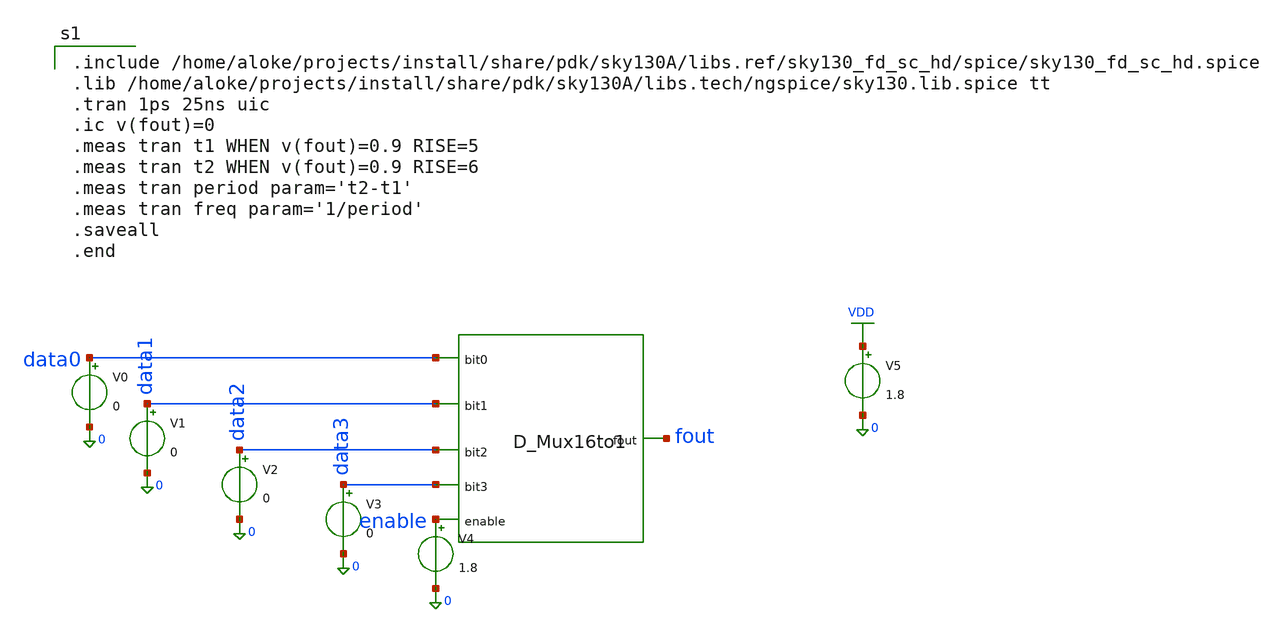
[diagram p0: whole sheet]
** sch_path: xschem/D_Mux16to1_tb.sch
**.subckt D_Mux16to1_tb
x1 data0 data1 enable data2 data3 fout D_Mux16to1
V0 data0 0 0
V1 data1 0 0
V2 data2 0 0
V3 data3 0 0
V5 VDD 0 1.8
V4 enable 0 1.8
**** begin user architecture code

.include /home/aloke/projects/install/share/pdk/sky130A/libs.ref/sky130_fd_sc_hd/spice/sky130_fd_sc_hd.spice
.lib /home/aloke/projects/install/share/pdk/sky130A/libs.tech/ngspice/sky130.lib.spice tt
.tran 1ps 25ns uic
.ic v(fout)=0
.meas tran t1 WHEN v(fout)=0.9 RISE=5
.meas tran t2 WHEN v(fout)=0.9 RISE=6
.meas tran period param='t2-t1'
.meas tran freq param='1/period'
.saveall
.end


**** end user architecture code
**.ends

* expanding   symbol:  D_Mux16to1.sym # of pins=6
** sym_path: xschem/D_Mux16to1.sym
** sch_path: xschem/D_Mux16to1.sch
.subckt D_Mux16to1 bit0 bit1 enable bit2 bit3 fout
*.ipin bit0
*.ipin bit1
*.ipin enable
*.ipin bit2
*.ipin bit3
*.opin fout
x37 net21 net22 net23 net24 net3 net4 VSS VSS VDD VDD net5 sky130_fd_sc_hd__mux4_1
x40 bit0 enable VSS VSS VDD VDD net3 sky130_fd_sc_hd__dlxtp_1
x1 fout VSS VSS VDD VDD net25 sky130_fd_sc_hd__clkinv_1
x36 net17 net18 net19 net20 net3 net4 VSS VSS VDD VDD net6 sky130_fd_sc_hd__mux4_1
x35 net13 net14 net15 net16 net3 net4 VSS VSS VDD VDD net7 sky130_fd_sc_hd__mux4_1
x34 net9 net10 net11 net12 net3 net4 VSS VSS VDD VDD net8 sky130_fd_sc_hd__mux4_1
x38 net8 net7 net6 net5 net1 net2 VSS VSS VDD VDD fout sky130_fd_sc_hd__mux4_1
x41 bit1 enable VSS VSS VDD VDD net4 sky130_fd_sc_hd__dlxtp_1
x42 bit2 enable VSS VSS VDD VDD net1 sky130_fd_sc_hd__dlxtp_1
x43 bit3 enable VSS VSS VDD VDD net2 sky130_fd_sc_hd__dlxtp_1
x2 net25 VSS VSS VDD VDD net26 sky130_fd_sc_hd__clkinv_1
x3 net26 VSS VSS VDD VDD net9 sky130_fd_sc_hd__clkinv_1
x4 net9 VSS VSS VDD VDD net27 sky130_fd_sc_hd__clkinv_1
x5 net27 VSS VSS VDD VDD net10 sky130_fd_sc_hd__clkinv_1
x7 net28 VSS VSS VDD VDD net11 sky130_fd_sc_hd__clkinv_1
x8 net11 VSS VSS VDD VDD net29 sky130_fd_sc_hd__clkinv_1
x9 net29 VSS VSS VDD VDD net12 sky130_fd_sc_hd__clkinv_1
x10 net12 VSS VSS VDD VDD net30 sky130_fd_sc_hd__clkinv_1
x12 net13 VSS VSS VDD VDD net31 sky130_fd_sc_hd__clkinv_1
x13 net31 VSS VSS VDD VDD net14 sky130_fd_sc_hd__clkinv_1
x14 net14 VSS VSS VDD VDD net32 sky130_fd_sc_hd__clkinv_1
x15 net32 VSS VSS VDD VDD net15 sky130_fd_sc_hd__clkinv_1
x16 net15 VSS VSS VDD VDD net33 sky130_fd_sc_hd__clkinv_1
x17 net33 VSS VSS VDD VDD net16 sky130_fd_sc_hd__clkinv_1
x19 net34 VSS VSS VDD VDD net17 sky130_fd_sc_hd__clkinv_1
x20 net17 VSS VSS VDD VDD net35 sky130_fd_sc_hd__clkinv_1
x6 net10 VSS VSS VDD VDD net28 sky130_fd_sc_hd__clkinv_1
x11 net30 VSS VSS VDD VDD net13 sky130_fd_sc_hd__clkinv_1
x18 net16 VSS VSS VDD VDD net34 sky130_fd_sc_hd__clkinv_1
x21 net35 VSS VSS VDD VDD net18 sky130_fd_sc_hd__clkinv_1
x22 net18 VSS VSS VDD VDD net36 sky130_fd_sc_hd__clkinv_1
x23 net36 VSS VSS VDD VDD net19 sky130_fd_sc_hd__clkinv_1
x24 net19 VSS VSS VDD VDD net37 sky130_fd_sc_hd__clkinv_1
x25 net37 VSS VSS VDD VDD net20 sky130_fd_sc_hd__clkinv_1
x26 net20 VSS VSS VDD VDD net38 sky130_fd_sc_hd__clkinv_1
x27 net38 VSS VSS VDD VDD net21 sky130_fd_sc_hd__clkinv_1
x28 net21 VSS VSS VDD VDD net39 sky130_fd_sc_hd__clkinv_1
x29 net39 VSS VSS VDD VDD net22 sky130_fd_sc_hd__clkinv_1
x30 net22 VSS VSS VDD VDD net40 sky130_fd_sc_hd__clkinv_1
x31 net40 VSS VSS VDD VDD net23 sky130_fd_sc_hd__clkinv_1
x32 net23 VSS VSS VDD VDD net41 sky130_fd_sc_hd__clkinv_1
x33 net41 VSS VSS VDD VDD net24 sky130_fd_sc_hd__clkinv_1
.ends

.GLOBAL VDD
.end
